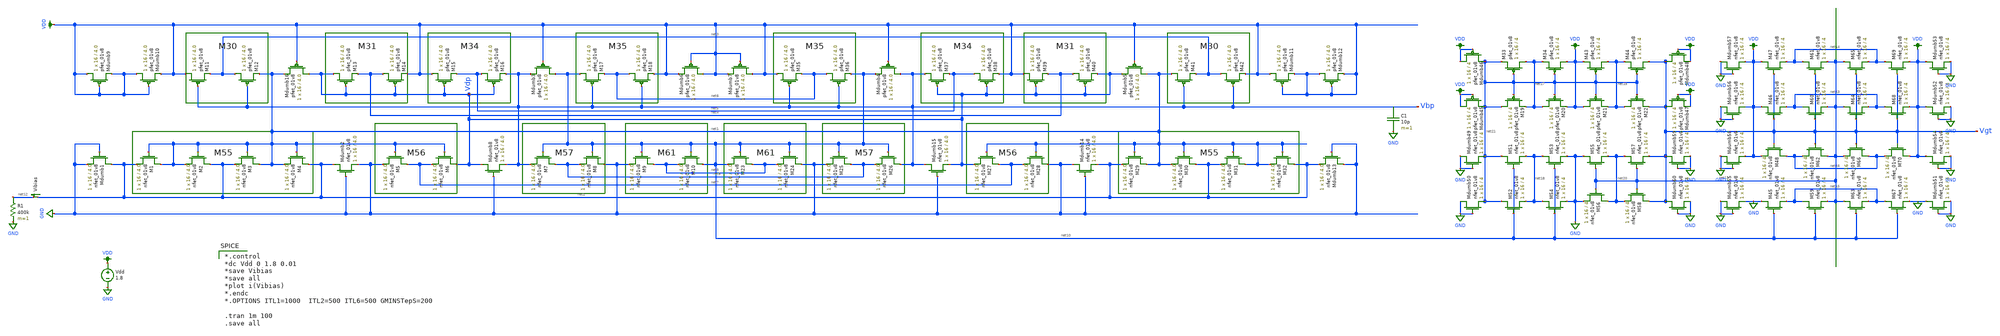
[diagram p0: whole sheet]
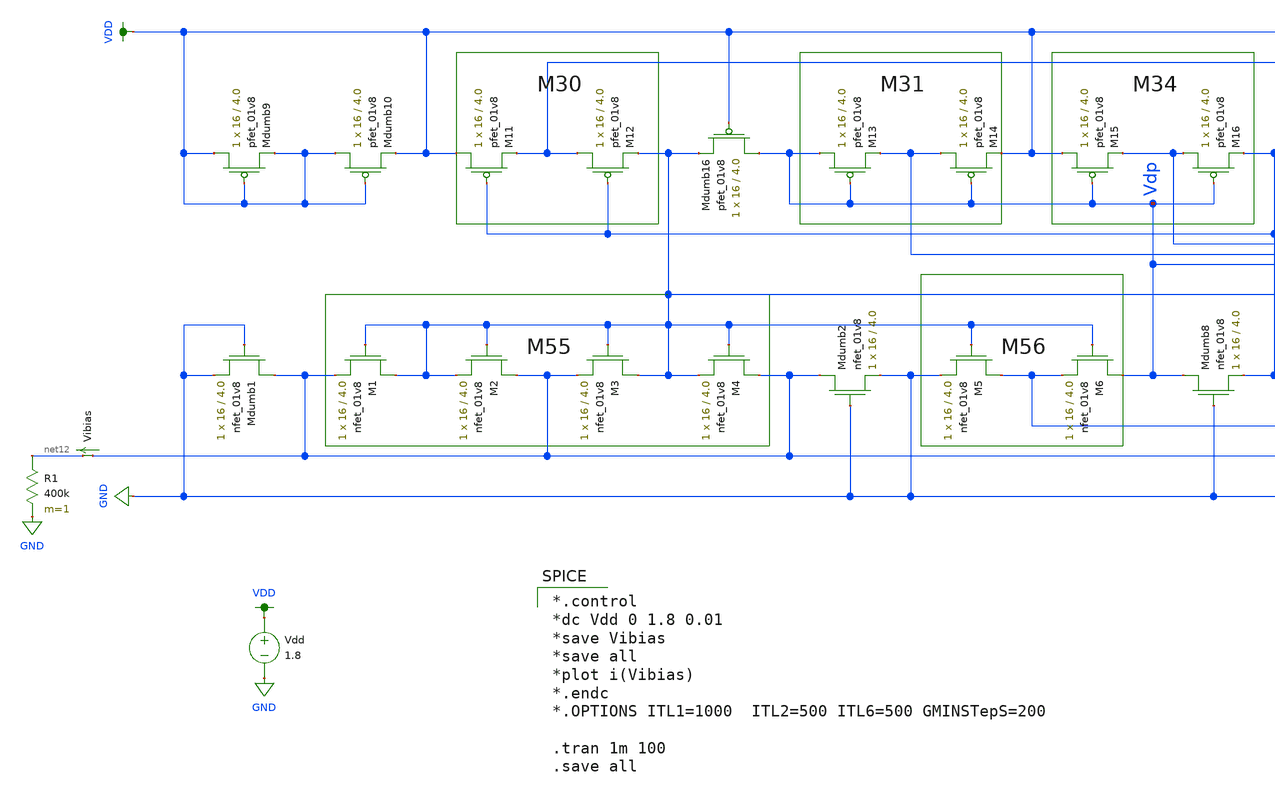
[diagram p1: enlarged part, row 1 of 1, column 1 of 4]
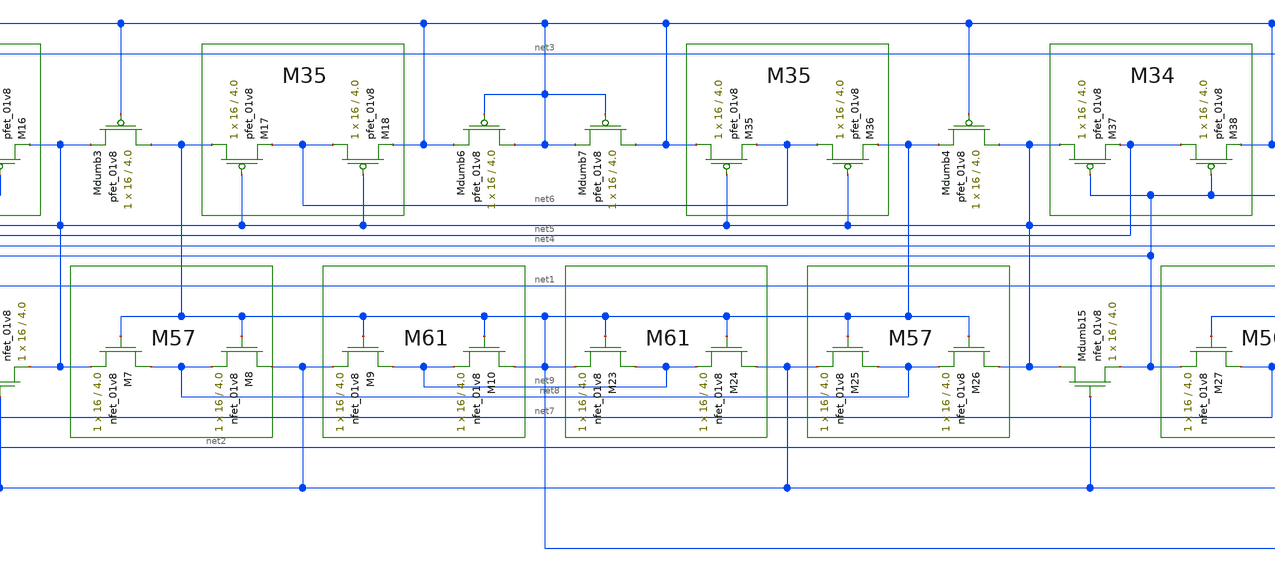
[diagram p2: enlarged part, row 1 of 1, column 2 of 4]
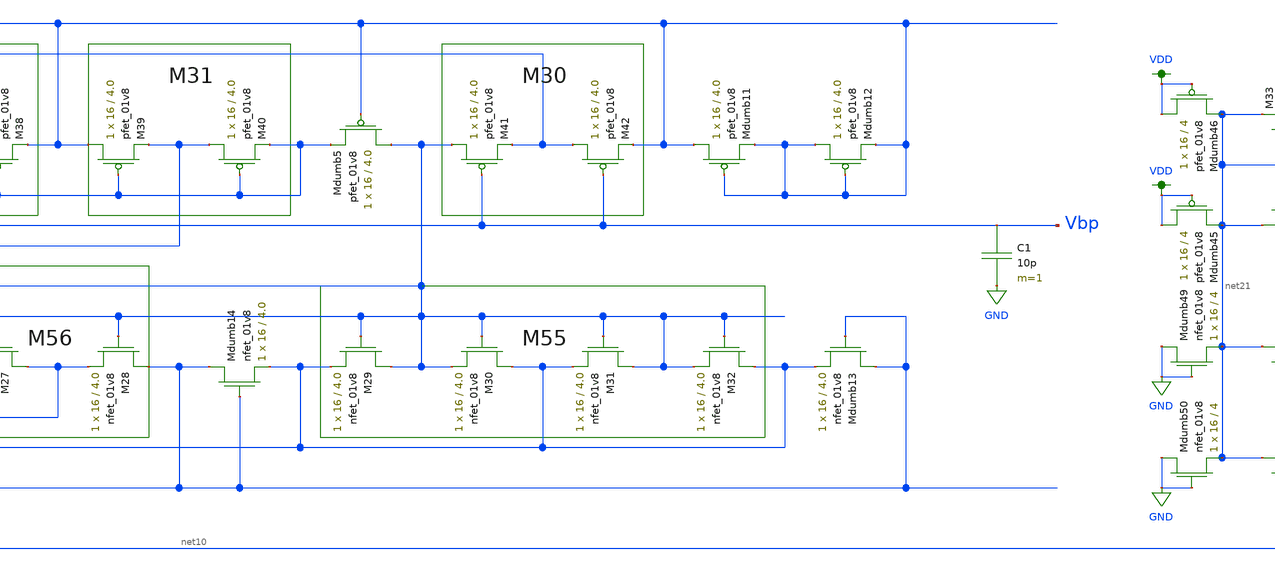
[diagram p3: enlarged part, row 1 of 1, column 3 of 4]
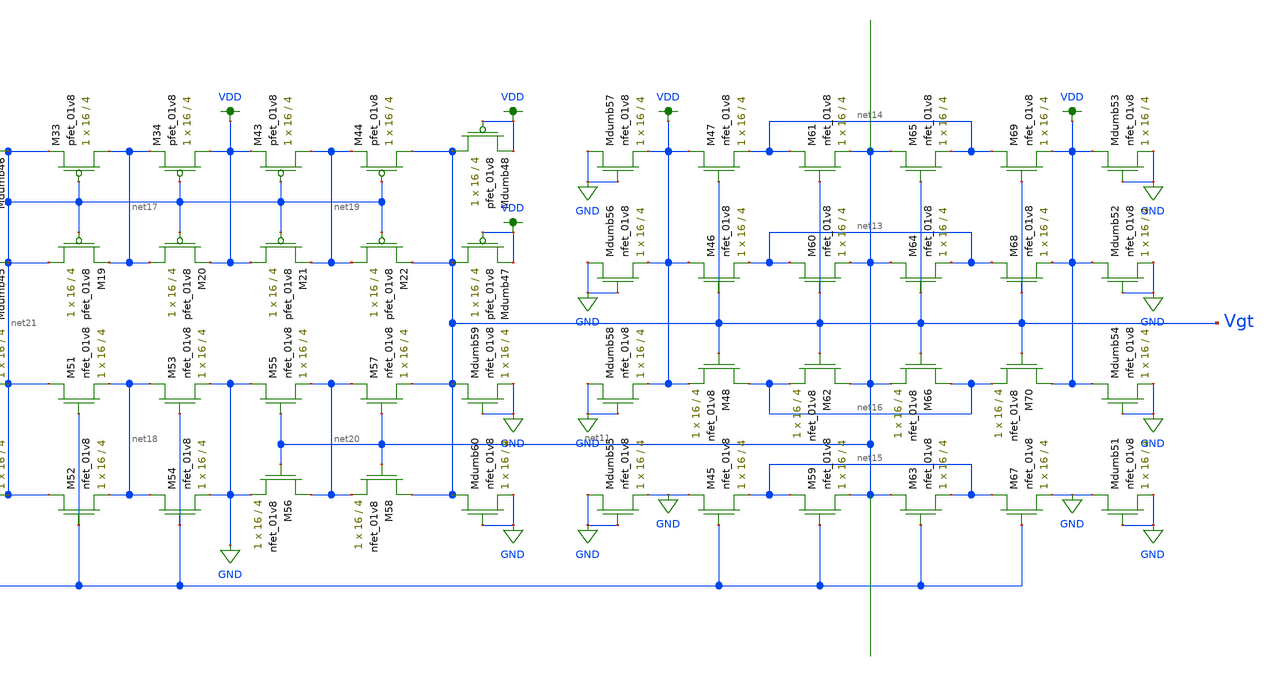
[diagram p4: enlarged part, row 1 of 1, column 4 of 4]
** sch_path: schematic/LDS/test/ibias_vgt.sch
**.subckt ibias_vgt
XM1 net1 net1 net2 GND sky130_fd_pr__nfet_01v8 L=4.0 W=16 nf=1 ad='int((nf+1)/2) * W/nf * 0.29' as='int((nf+2)/2) * W/nf * 0.29'
+ pd='2*int((nf+1)/2) * (W/nf + 0.29)' ps='2*int((nf+2)/2) * (W/nf + 0.29)' nrd='0.29 / W' nrs='0.29 / W'
+ sa=0 sb=0 sd=0 mult=1 m=1
XM2 net2 net1 net1 GND sky130_fd_pr__nfet_01v8 L=4.0 W=16 nf=1 ad='int((nf+1)/2) * W/nf * 0.29' as='int((nf+2)/2) * W/nf * 0.29'
+ pd='2*int((nf+1)/2) * (W/nf + 0.29)' ps='2*int((nf+2)/2) * (W/nf + 0.29)' nrd='0.29 / W' nrs='0.29 / W'
+ sa=0 sb=0 sd=0 mult=1 m=1
XM3 net1 net1 net2 GND sky130_fd_pr__nfet_01v8 L=4.0 W=16 nf=1 ad='int((nf+1)/2) * W/nf * 0.29' as='int((nf+2)/2) * W/nf * 0.29'
+ pd='2*int((nf+1)/2) * (W/nf + 0.29)' ps='2*int((nf+2)/2) * (W/nf + 0.29)' nrd='0.29 / W' nrs='0.29 / W'
+ sa=0 sb=0 sd=0 mult=1 m=1
XM4 net2 net1 net1 GND sky130_fd_pr__nfet_01v8 L=4.0 W=16 nf=1 ad='int((nf+1)/2) * W/nf * 0.29' as='int((nf+2)/2) * W/nf * 0.29'
+ pd='2*int((nf+1)/2) * (W/nf + 0.29)' ps='2*int((nf+2)/2) * (W/nf + 0.29)' nrd='0.29 / W' nrs='0.29 / W'
+ sa=0 sb=0 sd=0 mult=1 m=1
XM5 net7 net1 GND GND sky130_fd_pr__nfet_01v8 L=4.0 W=16 nf=1 ad='int((nf+1)/2) * W/nf * 0.29' as='int((nf+2)/2) * W/nf * 0.29'
+ pd='2*int((nf+1)/2) * (W/nf + 0.29)' ps='2*int((nf+2)/2) * (W/nf + 0.29)' nrd='0.29 / W' nrs='0.29 / W'
+ sa=0 sb=0 sd=0 mult=1 m=1
XM6 Vdp net1 net7 GND sky130_fd_pr__nfet_01v8 L=4.0 W=16 nf=1 ad='int((nf+1)/2) * W/nf * 0.29' as='int((nf+2)/2) * W/nf * 0.29'
+ pd='2*int((nf+1)/2) * (W/nf + 0.29)' ps='2*int((nf+2)/2) * (W/nf + 0.29)' nrd='0.29 / W' nrs='0.29 / W'
+ sa=0 sb=0 sd=0 mult=1 m=1
XM7 net8 net10 Vbp GND sky130_fd_pr__nfet_01v8 L=4.0 W=16 nf=1 ad='int((nf+1)/2) * W/nf * 0.29' as='int((nf+2)/2) * W/nf * 0.29'
+ pd='2*int((nf+1)/2) * (W/nf + 0.29)' ps='2*int((nf+2)/2) * (W/nf + 0.29)' nrd='0.29 / W' nrs='0.29 / W'
+ sa=0 sb=0 sd=0 mult=1 m=1
XM8 GND net10 net8 GND sky130_fd_pr__nfet_01v8 L=4.0 W=16 nf=1 ad='int((nf+1)/2) * W/nf * 0.29' as='int((nf+2)/2) * W/nf * 0.29'
+ pd='2*int((nf+1)/2) * (W/nf + 0.29)' ps='2*int((nf+2)/2) * (W/nf + 0.29)' nrd='0.29 / W' nrs='0.29 / W'
+ sa=0 sb=0 sd=0 mult=1 m=1
XM9 net9 net10 GND GND sky130_fd_pr__nfet_01v8 L=4.0 W=16 nf=1 ad='int((nf+1)/2) * W/nf * 0.29' as='int((nf+2)/2) * W/nf * 0.29'
+ pd='2*int((nf+1)/2) * (W/nf + 0.29)' ps='2*int((nf+2)/2) * (W/nf + 0.29)' nrd='0.29 / W' nrs='0.29 / W'
+ sa=0 sb=0 sd=0 mult=1 m=1
XM10 net10 net10 net9 GND sky130_fd_pr__nfet_01v8 L=4.0 W=16 nf=1 ad='int((nf+1)/2) * W/nf * 0.29' as='int((nf+2)/2) * W/nf * 0.29'
+ pd='2*int((nf+1)/2) * (W/nf + 0.29)' ps='2*int((nf+2)/2) * (W/nf + 0.29)' nrd='0.29 / W' nrs='0.29 / W'
+ sa=0 sb=0 sd=0 mult=1 m=1
XM11 VDD Vbp net3 VDD sky130_fd_pr__pfet_01v8 L=4.0 W=16 nf=1 ad='int((nf+1)/2) * W/nf * 0.29' as='int((nf+2)/2) * W/nf * 0.29'
+ pd='2*int((nf+1)/2) * (W/nf + 0.29)' ps='2*int((nf+2)/2) * (W/nf + 0.29)' nrd='0.29 / W' nrs='0.29 / W'
+ sa=0 sb=0 sd=0 mult=1 m=1
XM12 net3 Vbp net1 VDD sky130_fd_pr__pfet_01v8 L=4.0 W=16 nf=1 ad='int((nf+1)/2) * W/nf * 0.29' as='int((nf+2)/2) * W/nf * 0.29'
+ pd='2*int((nf+1)/2) * (W/nf + 0.29)' ps='2*int((nf+2)/2) * (W/nf + 0.29)' nrd='0.29 / W' nrs='0.29 / W'
+ sa=0 sb=0 sd=0 mult=1 m=1
XM13 Vdp Vdp net4 VDD sky130_fd_pr__pfet_01v8 L=4.0 W=16 nf=1 ad='int((nf+1)/2) * W/nf * 0.29' as='int((nf+2)/2) * W/nf * 0.29'
+ pd='2*int((nf+1)/2) * (W/nf + 0.29)' ps='2*int((nf+2)/2) * (W/nf + 0.29)' nrd='0.29 / W' nrs='0.29 / W'
+ sa=0 sb=0 sd=0 mult=1 m=1
XM14 net4 Vdp VDD VDD sky130_fd_pr__pfet_01v8 L=4.0 W=16 nf=1 ad='int((nf+1)/2) * W/nf * 0.29' as='int((nf+2)/2) * W/nf * 0.29'
+ pd='2*int((nf+1)/2) * (W/nf + 0.29)' ps='2*int((nf+2)/2) * (W/nf + 0.29)' nrd='0.29 / W' nrs='0.29 / W'
+ sa=0 sb=0 sd=0 mult=1 m=1
XM15 VDD Vdp net5 VDD sky130_fd_pr__pfet_01v8 L=4.0 W=16 nf=1 ad='int((nf+1)/2) * W/nf * 0.29' as='int((nf+2)/2) * W/nf * 0.29'
+ pd='2*int((nf+1)/2) * (W/nf + 0.29)' ps='2*int((nf+2)/2) * (W/nf + 0.29)' nrd='0.29 / W' nrs='0.29 / W'
+ sa=0 sb=0 sd=0 mult=1 m=1
XM16 net5 Vdp Vbp VDD sky130_fd_pr__pfet_01v8 L=4.0 W=16 nf=1 ad='int((nf+1)/2) * W/nf * 0.29' as='int((nf+2)/2) * W/nf * 0.29'
+ pd='2*int((nf+1)/2) * (W/nf + 0.29)' ps='2*int((nf+2)/2) * (W/nf + 0.29)' nrd='0.29 / W' nrs='0.29 / W'
+ sa=0 sb=0 sd=0 mult=1 m=1
XM17 net10 Vbp net6 VDD sky130_fd_pr__pfet_01v8 L=4.0 W=16 nf=1 ad='int((nf+1)/2) * W/nf * 0.29' as='int((nf+2)/2) * W/nf * 0.29'
+ pd='2*int((nf+1)/2) * (W/nf + 0.29)' ps='2*int((nf+2)/2) * (W/nf + 0.29)' nrd='0.29 / W' nrs='0.29 / W'
+ sa=0 sb=0 sd=0 mult=1 m=1
XM18 net6 Vbp VDD VDD sky130_fd_pr__pfet_01v8 L=4.0 W=16 nf=1 ad='int((nf+1)/2) * W/nf * 0.29' as='int((nf+2)/2) * W/nf * 0.29'
+ pd='2*int((nf+1)/2) * (W/nf + 0.29)' ps='2*int((nf+2)/2) * (W/nf + 0.29)' nrd='0.29 / W' nrs='0.29 / W'
+ sa=0 sb=0 sd=0 mult=1 m=1
XMdumb16 Vdp VDD net1 VDD sky130_fd_pr__pfet_01v8 L=4.0 W=16 nf=1 ad='int((nf+1)/2) * W/nf * 0.29' as='int((nf+2)/2) * W/nf * 0.29'
+ pd='2*int((nf+1)/2) * (W/nf + 0.29)' ps='2*int((nf+2)/2) * (W/nf + 0.29)' nrd='0.29 / W' nrs='0.29 / W'
+ sa=0 sb=0 sd=0 mult=1 m=1
XMdumb3 net10 VDD Vbp VDD sky130_fd_pr__pfet_01v8 L=4.0 W=16 nf=1 ad='int((nf+1)/2) * W/nf * 0.29' as='int((nf+2)/2) * W/nf * 0.29'
+ pd='2*int((nf+1)/2) * (W/nf + 0.29)' ps='2*int((nf+2)/2) * (W/nf + 0.29)' nrd='0.29 / W' nrs='0.29 / W'
+ sa=0 sb=0 sd=0 mult=1 m=1
XMdumb2 net2 GND GND GND sky130_fd_pr__nfet_01v8 L=4.0 W=16 nf=1 ad='int((nf+1)/2) * W/nf * 0.29' as='int((nf+2)/2) * W/nf * 0.29'
+ pd='2*int((nf+1)/2) * (W/nf + 0.29)' ps='2*int((nf+2)/2) * (W/nf + 0.29)' nrd='0.29 / W' nrs='0.29 / W'
+ sa=0 sb=0 sd=0 mult=1 m=1
XMdumb8 Vdp GND Vbp GND sky130_fd_pr__nfet_01v8 L=4.0 W=16 nf=1 ad='int((nf+1)/2) * W/nf * 0.29' as='int((nf+2)/2) * W/nf * 0.29'
+ pd='2*int((nf+1)/2) * (W/nf + 0.29)' ps='2*int((nf+2)/2) * (W/nf + 0.29)' nrd='0.29 / W' nrs='0.29 / W'
+ sa=0 sb=0 sd=0 mult=1 m=1
XM23 net9 net10 net10 GND sky130_fd_pr__nfet_01v8 L=4.0 W=16 nf=1 ad='int((nf+1)/2) * W/nf * 0.29' as='int((nf+2)/2) * W/nf * 0.29'
+ pd='2*int((nf+1)/2) * (W/nf + 0.29)' ps='2*int((nf+2)/2) * (W/nf + 0.29)' nrd='0.29 / W' nrs='0.29 / W'
+ sa=0 sb=0 sd=0 mult=1 m=1
XM24 GND net10 net9 GND sky130_fd_pr__nfet_01v8 L=4.0 W=16 nf=1 ad='int((nf+1)/2) * W/nf * 0.29' as='int((nf+2)/2) * W/nf * 0.29'
+ pd='2*int((nf+1)/2) * (W/nf + 0.29)' ps='2*int((nf+2)/2) * (W/nf + 0.29)' nrd='0.29 / W' nrs='0.29 / W'
+ sa=0 sb=0 sd=0 mult=1 m=1
XM25 net8 net10 GND GND sky130_fd_pr__nfet_01v8 L=4.0 W=16 nf=1 ad='int((nf+1)/2) * W/nf * 0.29' as='int((nf+2)/2) * W/nf * 0.29'
+ pd='2*int((nf+1)/2) * (W/nf + 0.29)' ps='2*int((nf+2)/2) * (W/nf + 0.29)' nrd='0.29 / W' nrs='0.29 / W'
+ sa=0 sb=0 sd=0 mult=1 m=1
XM26 Vbp net10 net8 GND sky130_fd_pr__nfet_01v8 L=4.0 W=16 nf=1 ad='int((nf+1)/2) * W/nf * 0.29' as='int((nf+2)/2) * W/nf * 0.29'
+ pd='2*int((nf+1)/2) * (W/nf + 0.29)' ps='2*int((nf+2)/2) * (W/nf + 0.29)' nrd='0.29 / W' nrs='0.29 / W'
+ sa=0 sb=0 sd=0 mult=1 m=1
XM27 net7 net1 Vdp GND sky130_fd_pr__nfet_01v8 L=4.0 W=16 nf=1 ad='int((nf+1)/2) * W/nf * 0.29' as='int((nf+2)/2) * W/nf * 0.29'
+ pd='2*int((nf+1)/2) * (W/nf + 0.29)' ps='2*int((nf+2)/2) * (W/nf + 0.29)' nrd='0.29 / W' nrs='0.29 / W'
+ sa=0 sb=0 sd=0 mult=1 m=1
XM28 GND net1 net7 GND sky130_fd_pr__nfet_01v8 L=4.0 W=16 nf=1 ad='int((nf+1)/2) * W/nf * 0.29' as='int((nf+2)/2) * W/nf * 0.29'
+ pd='2*int((nf+1)/2) * (W/nf + 0.29)' ps='2*int((nf+2)/2) * (W/nf + 0.29)' nrd='0.29 / W' nrs='0.29 / W'
+ sa=0 sb=0 sd=0 mult=1 m=1
XM29 net1 net1 net2 GND sky130_fd_pr__nfet_01v8 L=4.0 W=16 nf=1 ad='int((nf+1)/2) * W/nf * 0.29' as='int((nf+2)/2) * W/nf * 0.29'
+ pd='2*int((nf+1)/2) * (W/nf + 0.29)' ps='2*int((nf+2)/2) * (W/nf + 0.29)' nrd='0.29 / W' nrs='0.29 / W'
+ sa=0 sb=0 sd=0 mult=1 m=1
XM30 net2 net1 net1 GND sky130_fd_pr__nfet_01v8 L=4.0 W=16 nf=1 ad='int((nf+1)/2) * W/nf * 0.29' as='int((nf+2)/2) * W/nf * 0.29'
+ pd='2*int((nf+1)/2) * (W/nf + 0.29)' ps='2*int((nf+2)/2) * (W/nf + 0.29)' nrd='0.29 / W' nrs='0.29 / W'
+ sa=0 sb=0 sd=0 mult=1 m=1
XM31 net1 net1 net2 GND sky130_fd_pr__nfet_01v8 L=4.0 W=16 nf=1 ad='int((nf+1)/2) * W/nf * 0.29' as='int((nf+2)/2) * W/nf * 0.29'
+ pd='2*int((nf+1)/2) * (W/nf + 0.29)' ps='2*int((nf+2)/2) * (W/nf + 0.29)' nrd='0.29 / W' nrs='0.29 / W'
+ sa=0 sb=0 sd=0 mult=1 m=1
XM32 net2 net1 net1 GND sky130_fd_pr__nfet_01v8 L=4.0 W=16 nf=1 ad='int((nf+1)/2) * W/nf * 0.29' as='int((nf+2)/2) * W/nf * 0.29'
+ pd='2*int((nf+1)/2) * (W/nf + 0.29)' ps='2*int((nf+2)/2) * (W/nf + 0.29)' nrd='0.29 / W' nrs='0.29 / W'
+ sa=0 sb=0 sd=0 mult=1 m=1
XMdumb15 Vbp GND Vdp GND sky130_fd_pr__nfet_01v8 L=4.0 W=16 nf=1 ad='int((nf+1)/2) * W/nf * 0.29' as='int((nf+2)/2) * W/nf * 0.29'
+ pd='2*int((nf+1)/2) * (W/nf + 0.29)' ps='2*int((nf+2)/2) * (W/nf + 0.29)' nrd='0.29 / W' nrs='0.29 / W'
+ sa=0 sb=0 sd=0 mult=1 m=1
XMdumb14 GND GND net2 GND sky130_fd_pr__nfet_01v8 L=4.0 W=16 nf=1 ad='int((nf+1)/2) * W/nf * 0.29' as='int((nf+2)/2) * W/nf * 0.29'
+ pd='2*int((nf+1)/2) * (W/nf + 0.29)' ps='2*int((nf+2)/2) * (W/nf + 0.29)' nrd='0.29 / W' nrs='0.29 / W'
+ sa=0 sb=0 sd=0 mult=1 m=1
XM35 VDD Vbp net6 VDD sky130_fd_pr__pfet_01v8 L=4.0 W=16 nf=1 ad='int((nf+1)/2) * W/nf * 0.29' as='int((nf+2)/2) * W/nf * 0.29'
+ pd='2*int((nf+1)/2) * (W/nf + 0.29)' ps='2*int((nf+2)/2) * (W/nf + 0.29)' nrd='0.29 / W' nrs='0.29 / W'
+ sa=0 sb=0 sd=0 mult=1 m=1
XM36 net6 Vbp net10 VDD sky130_fd_pr__pfet_01v8 L=4.0 W=16 nf=1 ad='int((nf+1)/2) * W/nf * 0.29' as='int((nf+2)/2) * W/nf * 0.29'
+ pd='2*int((nf+1)/2) * (W/nf + 0.29)' ps='2*int((nf+2)/2) * (W/nf + 0.29)' nrd='0.29 / W' nrs='0.29 / W'
+ sa=0 sb=0 sd=0 mult=1 m=1
XM37 Vbp Vdp net5 VDD sky130_fd_pr__pfet_01v8 L=4.0 W=16 nf=1 ad='int((nf+1)/2) * W/nf * 0.29' as='int((nf+2)/2) * W/nf * 0.29'
+ pd='2*int((nf+1)/2) * (W/nf + 0.29)' ps='2*int((nf+2)/2) * (W/nf + 0.29)' nrd='0.29 / W' nrs='0.29 / W'
+ sa=0 sb=0 sd=0 mult=1 m=1
XM38 net5 Vdp VDD VDD sky130_fd_pr__pfet_01v8 L=4.0 W=16 nf=1 ad='int((nf+1)/2) * W/nf * 0.29' as='int((nf+2)/2) * W/nf * 0.29'
+ pd='2*int((nf+1)/2) * (W/nf + 0.29)' ps='2*int((nf+2)/2) * (W/nf + 0.29)' nrd='0.29 / W' nrs='0.29 / W'
+ sa=0 sb=0 sd=0 mult=1 m=1
XM39 VDD Vdp net4 VDD sky130_fd_pr__pfet_01v8 L=4.0 W=16 nf=1 ad='int((nf+1)/2) * W/nf * 0.29' as='int((nf+2)/2) * W/nf * 0.29'
+ pd='2*int((nf+1)/2) * (W/nf + 0.29)' ps='2*int((nf+2)/2) * (W/nf + 0.29)' nrd='0.29 / W' nrs='0.29 / W'
+ sa=0 sb=0 sd=0 mult=1 m=1
XM40 net4 Vdp Vdp VDD sky130_fd_pr__pfet_01v8 L=4.0 W=16 nf=1 ad='int((nf+1)/2) * W/nf * 0.29' as='int((nf+2)/2) * W/nf * 0.29'
+ pd='2*int((nf+1)/2) * (W/nf + 0.29)' ps='2*int((nf+2)/2) * (W/nf + 0.29)' nrd='0.29 / W' nrs='0.29 / W'
+ sa=0 sb=0 sd=0 mult=1 m=1
XM41 net1 Vbp net3 VDD sky130_fd_pr__pfet_01v8 L=4.0 W=16 nf=1 ad='int((nf+1)/2) * W/nf * 0.29' as='int((nf+2)/2) * W/nf * 0.29'
+ pd='2*int((nf+1)/2) * (W/nf + 0.29)' ps='2*int((nf+2)/2) * (W/nf + 0.29)' nrd='0.29 / W' nrs='0.29 / W'
+ sa=0 sb=0 sd=0 mult=1 m=1
XM42 net3 Vbp VDD VDD sky130_fd_pr__pfet_01v8 L=4.0 W=16 nf=1 ad='int((nf+1)/2) * W/nf * 0.29' as='int((nf+2)/2) * W/nf * 0.29'
+ pd='2*int((nf+1)/2) * (W/nf + 0.29)' ps='2*int((nf+2)/2) * (W/nf + 0.29)' nrd='0.29 / W' nrs='0.29 / W'
+ sa=0 sb=0 sd=0 mult=1 m=1
XMdumb4 Vbp VDD net10 VDD sky130_fd_pr__pfet_01v8 L=4.0 W=16 nf=1 ad='int((nf+1)/2) * W/nf * 0.29' as='int((nf+2)/2) * W/nf * 0.29'
+ pd='2*int((nf+1)/2) * (W/nf + 0.29)' ps='2*int((nf+2)/2) * (W/nf + 0.29)' nrd='0.29 / W' nrs='0.29 / W'
+ sa=0 sb=0 sd=0 mult=1 m=1
XMdumb5 net1 VDD Vdp VDD sky130_fd_pr__pfet_01v8 L=4.0 W=16 nf=1 ad='int((nf+1)/2) * W/nf * 0.29' as='int((nf+2)/2) * W/nf * 0.29'
+ pd='2*int((nf+1)/2) * (W/nf + 0.29)' ps='2*int((nf+2)/2) * (W/nf + 0.29)' nrd='0.29 / W' nrs='0.29 / W'
+ sa=0 sb=0 sd=0 mult=1 m=1
XMdumb6 VDD VDD VDD VDD sky130_fd_pr__pfet_01v8 L=4.0 W=16 nf=1 ad='int((nf+1)/2) * W/nf * 0.29' as='int((nf+2)/2) * W/nf * 0.29'
+ pd='2*int((nf+1)/2) * (W/nf + 0.29)' ps='2*int((nf+2)/2) * (W/nf + 0.29)' nrd='0.29 / W' nrs='0.29 / W'
+ sa=0 sb=0 sd=0 mult=1 m=1
XMdumb7 VDD VDD VDD VDD sky130_fd_pr__pfet_01v8 L=4.0 W=16 nf=1 ad='int((nf+1)/2) * W/nf * 0.29' as='int((nf+2)/2) * W/nf * 0.29'
+ pd='2*int((nf+1)/2) * (W/nf + 0.29)' ps='2*int((nf+2)/2) * (W/nf + 0.29)' nrd='0.29 / W' nrs='0.29 / W'
+ sa=0 sb=0 sd=0 mult=1 m=1
XMdumb11 VDD VDD VDD VDD sky130_fd_pr__pfet_01v8 L=4.0 W=16 nf=1 ad='int((nf+1)/2) * W/nf * 0.29' as='int((nf+2)/2) * W/nf * 0.29'
+ pd='2*int((nf+1)/2) * (W/nf + 0.29)' ps='2*int((nf+2)/2) * (W/nf + 0.29)' nrd='0.29 / W' nrs='0.29 / W'
+ sa=0 sb=0 sd=0 mult=1 m=1
XMdumb12 VDD VDD VDD VDD sky130_fd_pr__pfet_01v8 L=4.0 W=16 nf=1 ad='int((nf+1)/2) * W/nf * 0.29' as='int((nf+2)/2) * W/nf * 0.29'
+ pd='2*int((nf+1)/2) * (W/nf + 0.29)' ps='2*int((nf+2)/2) * (W/nf + 0.29)' nrd='0.29 / W' nrs='0.29 / W'
+ sa=0 sb=0 sd=0 mult=1 m=1
XMdumb13 GND GND net2 GND sky130_fd_pr__nfet_01v8 L=4.0 W=16 nf=1 ad='int((nf+1)/2) * W/nf * 0.29' as='int((nf+2)/2) * W/nf * 0.29'
+ pd='2*int((nf+1)/2) * (W/nf + 0.29)' ps='2*int((nf+2)/2) * (W/nf + 0.29)' nrd='0.29 / W' nrs='0.29 / W'
+ sa=0 sb=0 sd=0 mult=1 m=1
XMdumb1 net2 GND GND GND sky130_fd_pr__nfet_01v8 L=4.0 W=16 nf=1 ad='int((nf+1)/2) * W/nf * 0.29' as='int((nf+2)/2) * W/nf * 0.29'
+ pd='2*int((nf+1)/2) * (W/nf + 0.29)' ps='2*int((nf+2)/2) * (W/nf + 0.29)' nrd='0.29 / W' nrs='0.29 / W'
+ sa=0 sb=0 sd=0 mult=1 m=1
XMdumb10 VDD VDD VDD VDD sky130_fd_pr__pfet_01v8 L=4.0 W=16 nf=1 ad='int((nf+1)/2) * W/nf * 0.29' as='int((nf+2)/2) * W/nf * 0.29'
+ pd='2*int((nf+1)/2) * (W/nf + 0.29)' ps='2*int((nf+2)/2) * (W/nf + 0.29)' nrd='0.29 / W' nrs='0.29 / W'
+ sa=0 sb=0 sd=0 mult=1 m=1
XMdumb9 VDD VDD VDD VDD sky130_fd_pr__pfet_01v8 L=4.0 W=16 nf=1 ad='int((nf+1)/2) * W/nf * 0.29' as='int((nf+2)/2) * W/nf * 0.29'
+ pd='2*int((nf+1)/2) * (W/nf + 0.29)' ps='2*int((nf+2)/2) * (W/nf + 0.29)' nrd='0.29 / W' nrs='0.29 / W'
+ sa=0 sb=0 sd=0 mult=1 m=1
Vdd VDD GND 1.8
R1 net12 GND 400k m=1
Vibias net2 net12 0
.save i(vibias)
XM45 GND net10 net15 GND sky130_fd_pr__nfet_01v8 L=4 W=16 nf=1 ad='int((nf+1)/2) * W/nf * 0.29' as='int((nf+2)/2) * W/nf * 0.29'
+ pd='2*int((nf+1)/2) * (W/nf + 0.29)' ps='2*int((nf+2)/2) * (W/nf + 0.29)' nrd='0.29 / W' nrs='0.29 / W'
+ sa=0 sb=0 sd=0 mult=1 m=1
XM46 VDD Vgt net13 GND sky130_fd_pr__nfet_01v8 L=4 W=16 nf=1 ad='int((nf+1)/2) * W/nf * 0.29' as='int((nf+2)/2) * W/nf * 0.29'
+ pd='2*int((nf+1)/2) * (W/nf + 0.29)' ps='2*int((nf+2)/2) * (W/nf + 0.29)' nrd='0.29 / W' nrs='0.29 / W'
+ sa=0 sb=0 sd=0 mult=1 m=1
XM47 VDD Vgt net14 GND sky130_fd_pr__nfet_01v8 L=4 W=16 nf=1 ad='int((nf+1)/2) * W/nf * 0.29' as='int((nf+2)/2) * W/nf * 0.29'
+ pd='2*int((nf+1)/2) * (W/nf + 0.29)' ps='2*int((nf+2)/2) * (W/nf + 0.29)' nrd='0.29 / W' nrs='0.29 / W'
+ sa=0 sb=0 sd=0 mult=1 m=1
XM48 net16 Vgt VDD GND sky130_fd_pr__nfet_01v8 L=4 W=16 nf=1 ad='int((nf+1)/2) * W/nf * 0.29' as='int((nf+2)/2) * W/nf * 0.29'
+ pd='2*int((nf+1)/2) * (W/nf + 0.29)' ps='2*int((nf+2)/2) * (W/nf + 0.29)' nrd='0.29 / W' nrs='0.29 / W'
+ sa=0 sb=0 sd=0 mult=1 m=1
XMdumb51 GND GND GND GND sky130_fd_pr__nfet_01v8 L=4 W=16 nf=1 ad='int((nf+1)/2) * W/nf * 0.29' as='int((nf+2)/2) * W/nf * 0.29'
+ pd='2*int((nf+1)/2) * (W/nf + 0.29)' ps='2*int((nf+2)/2) * (W/nf + 0.29)' nrd='0.29 / W' nrs='0.29 / W'
+ sa=0 sb=0 sd=0 mult=1 m=1
XMdumb52 VDD GND GND GND sky130_fd_pr__nfet_01v8 L=4 W=16 nf=1 ad='int((nf+1)/2) * W/nf * 0.29' as='int((nf+2)/2) * W/nf * 0.29'
+ pd='2*int((nf+1)/2) * (W/nf + 0.29)' ps='2*int((nf+2)/2) * (W/nf + 0.29)' nrd='0.29 / W' nrs='0.29 / W'
+ sa=0 sb=0 sd=0 mult=1 m=1
XMdumb53 VDD GND GND GND sky130_fd_pr__nfet_01v8 L=4 W=16 nf=1 ad='int((nf+1)/2) * W/nf * 0.29' as='int((nf+2)/2) * W/nf * 0.29'
+ pd='2*int((nf+1)/2) * (W/nf + 0.29)' ps='2*int((nf+2)/2) * (W/nf + 0.29)' nrd='0.29 / W' nrs='0.29 / W'
+ sa=0 sb=0 sd=0 mult=1 m=1
XMdumb54 VDD GND GND GND sky130_fd_pr__nfet_01v8 L=4 W=16 nf=1 ad='int((nf+1)/2) * W/nf * 0.29' as='int((nf+2)/2) * W/nf * 0.29'
+ pd='2*int((nf+1)/2) * (W/nf + 0.29)' ps='2*int((nf+2)/2) * (W/nf + 0.29)' nrd='0.29 / W' nrs='0.29 / W'
+ sa=0 sb=0 sd=0 mult=1 m=1
XMdumb55 GND GND GND GND sky130_fd_pr__nfet_01v8 L=4 W=16 nf=1 ad='int((nf+1)/2) * W/nf * 0.29' as='int((nf+2)/2) * W/nf * 0.29'
+ pd='2*int((nf+1)/2) * (W/nf + 0.29)' ps='2*int((nf+2)/2) * (W/nf + 0.29)' nrd='0.29 / W' nrs='0.29 / W'
+ sa=0 sb=0 sd=0 mult=1 m=1
XMdumb56 GND GND VDD GND sky130_fd_pr__nfet_01v8 L=4 W=16 nf=1 ad='int((nf+1)/2) * W/nf * 0.29' as='int((nf+2)/2) * W/nf * 0.29'
+ pd='2*int((nf+1)/2) * (W/nf + 0.29)' ps='2*int((nf+2)/2) * (W/nf + 0.29)' nrd='0.29 / W' nrs='0.29 / W'
+ sa=0 sb=0 sd=0 mult=1 m=1
XMdumb57 GND GND VDD GND sky130_fd_pr__nfet_01v8 L=4 W=16 nf=1 ad='int((nf+1)/2) * W/nf * 0.29' as='int((nf+2)/2) * W/nf * 0.29'
+ pd='2*int((nf+1)/2) * (W/nf + 0.29)' ps='2*int((nf+2)/2) * (W/nf + 0.29)' nrd='0.29 / W' nrs='0.29 / W'
+ sa=0 sb=0 sd=0 mult=1 m=1
XMdumb58 GND GND VDD GND sky130_fd_pr__nfet_01v8 L=4 W=16 nf=1 ad='int((nf+1)/2) * W/nf * 0.29' as='int((nf+2)/2) * W/nf * 0.29'
+ pd='2*int((nf+1)/2) * (W/nf + 0.29)' ps='2*int((nf+2)/2) * (W/nf + 0.29)' nrd='0.29 / W' nrs='0.29 / W'
+ sa=0 sb=0 sd=0 mult=1 m=1
XM59 net15 net10 net11 GND sky130_fd_pr__nfet_01v8 L=4 W=16 nf=1 ad='int((nf+1)/2) * W/nf * 0.29' as='int((nf+2)/2) * W/nf * 0.29'
+ pd='2*int((nf+1)/2) * (W/nf + 0.29)' ps='2*int((nf+2)/2) * (W/nf + 0.29)' nrd='0.29 / W' nrs='0.29 / W'
+ sa=0 sb=0 sd=0 mult=1 m=1
XM60 net13 Vgt net11 GND sky130_fd_pr__nfet_01v8 L=4 W=16 nf=1 ad='int((nf+1)/2) * W/nf * 0.29' as='int((nf+2)/2) * W/nf * 0.29'
+ pd='2*int((nf+1)/2) * (W/nf + 0.29)' ps='2*int((nf+2)/2) * (W/nf + 0.29)' nrd='0.29 / W' nrs='0.29 / W'
+ sa=0 sb=0 sd=0 mult=1 m=1
XM61 net14 Vgt net11 GND sky130_fd_pr__nfet_01v8 L=4 W=16 nf=1 ad='int((nf+1)/2) * W/nf * 0.29' as='int((nf+2)/2) * W/nf * 0.29'
+ pd='2*int((nf+1)/2) * (W/nf + 0.29)' ps='2*int((nf+2)/2) * (W/nf + 0.29)' nrd='0.29 / W' nrs='0.29 / W'
+ sa=0 sb=0 sd=0 mult=1 m=1
XM62 net11 Vgt net16 GND sky130_fd_pr__nfet_01v8 L=4 W=16 nf=1 ad='int((nf+1)/2) * W/nf * 0.29' as='int((nf+2)/2) * W/nf * 0.29'
+ pd='2*int((nf+1)/2) * (W/nf + 0.29)' ps='2*int((nf+2)/2) * (W/nf + 0.29)' nrd='0.29 / W' nrs='0.29 / W'
+ sa=0 sb=0 sd=0 mult=1 m=1
XM63 net11 net10 net15 GND sky130_fd_pr__nfet_01v8 L=4 W=16 nf=1 ad='int((nf+1)/2) * W/nf * 0.29' as='int((nf+2)/2) * W/nf * 0.29'
+ pd='2*int((nf+1)/2) * (W/nf + 0.29)' ps='2*int((nf+2)/2) * (W/nf + 0.29)' nrd='0.29 / W' nrs='0.29 / W'
+ sa=0 sb=0 sd=0 mult=1 m=1
XM64 net11 Vgt net13 GND sky130_fd_pr__nfet_01v8 L=4 W=16 nf=1 ad='int((nf+1)/2) * W/nf * 0.29' as='int((nf+2)/2) * W/nf * 0.29'
+ pd='2*int((nf+1)/2) * (W/nf + 0.29)' ps='2*int((nf+2)/2) * (W/nf + 0.29)' nrd='0.29 / W' nrs='0.29 / W'
+ sa=0 sb=0 sd=0 mult=1 m=1
XM65 net11 Vgt net14 GND sky130_fd_pr__nfet_01v8 L=4 W=16 nf=1 ad='int((nf+1)/2) * W/nf * 0.29' as='int((nf+2)/2) * W/nf * 0.29'
+ pd='2*int((nf+1)/2) * (W/nf + 0.29)' ps='2*int((nf+2)/2) * (W/nf + 0.29)' nrd='0.29 / W' nrs='0.29 / W'
+ sa=0 sb=0 sd=0 mult=1 m=1
XM66 net16 Vgt net11 GND sky130_fd_pr__nfet_01v8 L=4 W=16 nf=1 ad='int((nf+1)/2) * W/nf * 0.29' as='int((nf+2)/2) * W/nf * 0.29'
+ pd='2*int((nf+1)/2) * (W/nf + 0.29)' ps='2*int((nf+2)/2) * (W/nf + 0.29)' nrd='0.29 / W' nrs='0.29 / W'
+ sa=0 sb=0 sd=0 mult=1 m=1
XM67 net15 net10 GND GND sky130_fd_pr__nfet_01v8 L=4 W=16 nf=1 ad='int((nf+1)/2) * W/nf * 0.29' as='int((nf+2)/2) * W/nf * 0.29'
+ pd='2*int((nf+1)/2) * (W/nf + 0.29)' ps='2*int((nf+2)/2) * (W/nf + 0.29)' nrd='0.29 / W' nrs='0.29 / W'
+ sa=0 sb=0 sd=0 mult=1 m=1
XM68 net13 Vgt VDD GND sky130_fd_pr__nfet_01v8 L=4 W=16 nf=1 ad='int((nf+1)/2) * W/nf * 0.29' as='int((nf+2)/2) * W/nf * 0.29'
+ pd='2*int((nf+1)/2) * (W/nf + 0.29)' ps='2*int((nf+2)/2) * (W/nf + 0.29)' nrd='0.29 / W' nrs='0.29 / W'
+ sa=0 sb=0 sd=0 mult=1 m=1
XM69 net14 Vgt VDD GND sky130_fd_pr__nfet_01v8 L=4 W=16 nf=1 ad='int((nf+1)/2) * W/nf * 0.29' as='int((nf+2)/2) * W/nf * 0.29'
+ pd='2*int((nf+1)/2) * (W/nf + 0.29)' ps='2*int((nf+2)/2) * (W/nf + 0.29)' nrd='0.29 / W' nrs='0.29 / W'
+ sa=0 sb=0 sd=0 mult=1 m=1
XM70 VDD Vgt net16 GND sky130_fd_pr__nfet_01v8 L=4 W=16 nf=1 ad='int((nf+1)/2) * W/nf * 0.29' as='int((nf+2)/2) * W/nf * 0.29'
+ pd='2*int((nf+1)/2) * (W/nf + 0.29)' ps='2*int((nf+2)/2) * (W/nf + 0.29)' nrd='0.29 / W' nrs='0.29 / W'
+ sa=0 sb=0 sd=0 mult=1 m=1
XM19 net21 net21 net17 VDD sky130_fd_pr__pfet_01v8 L=4 W=16 nf=1 ad='int((nf+1)/2) * W/nf * 0.29' as='int((nf+2)/2) * W/nf * 0.29'
+ pd='2*int((nf+1)/2) * (W/nf + 0.29)' ps='2*int((nf+2)/2) * (W/nf + 0.29)' nrd='0.29 / W' nrs='0.29 / W'
+ sa=0 sb=0 sd=0 mult=1 m=1
XM20 net17 net21 VDD VDD sky130_fd_pr__pfet_01v8 L=4 W=16 nf=1 ad='int((nf+1)/2) * W/nf * 0.29' as='int((nf+2)/2) * W/nf * 0.29'
+ pd='2*int((nf+1)/2) * (W/nf + 0.29)' ps='2*int((nf+2)/2) * (W/nf + 0.29)' nrd='0.29 / W' nrs='0.29 / W'
+ sa=0 sb=0 sd=0 mult=1 m=1
XM21 VDD net21 net19 VDD sky130_fd_pr__pfet_01v8 L=4 W=16 nf=1 ad='int((nf+1)/2) * W/nf * 0.29' as='int((nf+2)/2) * W/nf * 0.29'
+ pd='2*int((nf+1)/2) * (W/nf + 0.29)' ps='2*int((nf+2)/2) * (W/nf + 0.29)' nrd='0.29 / W' nrs='0.29 / W'
+ sa=0 sb=0 sd=0 mult=1 m=1
XM22 net19 net21 Vgt VDD sky130_fd_pr__pfet_01v8 L=4 W=16 nf=1 ad='int((nf+1)/2) * W/nf * 0.29' as='int((nf+2)/2) * W/nf * 0.29'
+ pd='2*int((nf+1)/2) * (W/nf + 0.29)' ps='2*int((nf+2)/2) * (W/nf + 0.29)' nrd='0.29 / W' nrs='0.29 / W'
+ sa=0 sb=0 sd=0 mult=1 m=1
XM33 net17 net21 net21 VDD sky130_fd_pr__pfet_01v8 L=4 W=16 nf=1 ad='int((nf+1)/2) * W/nf * 0.29' as='int((nf+2)/2) * W/nf * 0.29'
+ pd='2*int((nf+1)/2) * (W/nf + 0.29)' ps='2*int((nf+2)/2) * (W/nf + 0.29)' nrd='0.29 / W' nrs='0.29 / W'
+ sa=0 sb=0 sd=0 mult=1 m=1
XM34 VDD net21 net17 VDD sky130_fd_pr__pfet_01v8 L=4 W=16 nf=1 ad='int((nf+1)/2) * W/nf * 0.29' as='int((nf+2)/2) * W/nf * 0.29'
+ pd='2*int((nf+1)/2) * (W/nf + 0.29)' ps='2*int((nf+2)/2) * (W/nf + 0.29)' nrd='0.29 / W' nrs='0.29 / W'
+ sa=0 sb=0 sd=0 mult=1 m=1
XM43 net19 net21 VDD VDD sky130_fd_pr__pfet_01v8 L=4 W=16 nf=1 ad='int((nf+1)/2) * W/nf * 0.29' as='int((nf+2)/2) * W/nf * 0.29'
+ pd='2*int((nf+1)/2) * (W/nf + 0.29)' ps='2*int((nf+2)/2) * (W/nf + 0.29)' nrd='0.29 / W' nrs='0.29 / W'
+ sa=0 sb=0 sd=0 mult=1 m=1
XM44 Vgt net21 net19 VDD sky130_fd_pr__pfet_01v8 L=4 W=16 nf=1 ad='int((nf+1)/2) * W/nf * 0.29' as='int((nf+2)/2) * W/nf * 0.29'
+ pd='2*int((nf+1)/2) * (W/nf + 0.29)' ps='2*int((nf+2)/2) * (W/nf + 0.29)' nrd='0.29 / W' nrs='0.29 / W'
+ sa=0 sb=0 sd=0 mult=1 m=1
XMdumb45 VDD VDD net21 VDD sky130_fd_pr__pfet_01v8 L=4 W=16 nf=1 ad='int((nf+1)/2) * W/nf * 0.29' as='int((nf+2)/2) * W/nf * 0.29'
+ pd='2*int((nf+1)/2) * (W/nf + 0.29)' ps='2*int((nf+2)/2) * (W/nf + 0.29)' nrd='0.29 / W' nrs='0.29 / W'
+ sa=0 sb=0 sd=0 mult=1 m=1
XMdumb46 VDD VDD net21 VDD sky130_fd_pr__pfet_01v8 L=4 W=16 nf=1 ad='int((nf+1)/2) * W/nf * 0.29' as='int((nf+2)/2) * W/nf * 0.29'
+ pd='2*int((nf+1)/2) * (W/nf + 0.29)' ps='2*int((nf+2)/2) * (W/nf + 0.29)' nrd='0.29 / W' nrs='0.29 / W'
+ sa=0 sb=0 sd=0 mult=1 m=1
XMdumb47 Vgt VDD VDD VDD sky130_fd_pr__pfet_01v8 L=4 W=16 nf=1 ad='int((nf+1)/2) * W/nf * 0.29' as='int((nf+2)/2) * W/nf * 0.29'
+ pd='2*int((nf+1)/2) * (W/nf + 0.29)' ps='2*int((nf+2)/2) * (W/nf + 0.29)' nrd='0.29 / W' nrs='0.29 / W'
+ sa=0 sb=0 sd=0 mult=1 m=1
XMdumb48 Vgt VDD VDD VDD sky130_fd_pr__pfet_01v8 L=4 W=16 nf=1 ad='int((nf+1)/2) * W/nf * 0.29' as='int((nf+2)/2) * W/nf * 0.29'
+ pd='2*int((nf+1)/2) * (W/nf + 0.29)' ps='2*int((nf+2)/2) * (W/nf + 0.29)' nrd='0.29 / W' nrs='0.29 / W'
+ sa=0 sb=0 sd=0 mult=1 m=1
XMdumb49 GND GND net21 GND sky130_fd_pr__nfet_01v8 L=4 W=16 nf=1 ad='int((nf+1)/2) * W/nf * 0.29' as='int((nf+2)/2) * W/nf * 0.29'
+ pd='2*int((nf+1)/2) * (W/nf + 0.29)' ps='2*int((nf+2)/2) * (W/nf + 0.29)' nrd='0.29 / W' nrs='0.29 / W'
+ sa=0 sb=0 sd=0 mult=1 m=1
XMdumb50 GND GND net21 GND sky130_fd_pr__nfet_01v8 L=4 W=16 nf=1 ad='int((nf+1)/2) * W/nf * 0.29' as='int((nf+2)/2) * W/nf * 0.29'
+ pd='2*int((nf+1)/2) * (W/nf + 0.29)' ps='2*int((nf+2)/2) * (W/nf + 0.29)' nrd='0.29 / W' nrs='0.29 / W'
+ sa=0 sb=0 sd=0 mult=1 m=1
XM51 net21 net10 net18 GND sky130_fd_pr__nfet_01v8 L=4 W=16 nf=1 ad='int((nf+1)/2) * W/nf * 0.29' as='int((nf+2)/2) * W/nf * 0.29'
+ pd='2*int((nf+1)/2) * (W/nf + 0.29)' ps='2*int((nf+2)/2) * (W/nf + 0.29)' nrd='0.29 / W' nrs='0.29 / W'
+ sa=0 sb=0 sd=0 mult=1 m=1
XM52 net21 net10 net18 GND sky130_fd_pr__nfet_01v8 L=4 W=16 nf=1 ad='int((nf+1)/2) * W/nf * 0.29' as='int((nf+2)/2) * W/nf * 0.29'
+ pd='2*int((nf+1)/2) * (W/nf + 0.29)' ps='2*int((nf+2)/2) * (W/nf + 0.29)' nrd='0.29 / W' nrs='0.29 / W'
+ sa=0 sb=0 sd=0 mult=1 m=1
XM53 net18 net10 GND GND sky130_fd_pr__nfet_01v8 L=4 W=16 nf=1 ad='int((nf+1)/2) * W/nf * 0.29' as='int((nf+2)/2) * W/nf * 0.29'
+ pd='2*int((nf+1)/2) * (W/nf + 0.29)' ps='2*int((nf+2)/2) * (W/nf + 0.29)' nrd='0.29 / W' nrs='0.29 / W'
+ sa=0 sb=0 sd=0 mult=1 m=1
XM54 net18 net10 GND GND sky130_fd_pr__nfet_01v8 L=4 W=16 nf=1 ad='int((nf+1)/2) * W/nf * 0.29' as='int((nf+2)/2) * W/nf * 0.29'
+ pd='2*int((nf+1)/2) * (W/nf + 0.29)' ps='2*int((nf+2)/2) * (W/nf + 0.29)' nrd='0.29 / W' nrs='0.29 / W'
+ sa=0 sb=0 sd=0 mult=1 m=1
XM55 GND net11 net20 GND sky130_fd_pr__nfet_01v8 L=4 W=16 nf=1 ad='int((nf+1)/2) * W/nf * 0.29' as='int((nf+2)/2) * W/nf * 0.29'
+ pd='2*int((nf+1)/2) * (W/nf + 0.29)' ps='2*int((nf+2)/2) * (W/nf + 0.29)' nrd='0.29 / W' nrs='0.29 / W'
+ sa=0 sb=0 sd=0 mult=1 m=1
XM56 net20 net11 GND GND sky130_fd_pr__nfet_01v8 L=4 W=16 nf=1 ad='int((nf+1)/2) * W/nf * 0.29' as='int((nf+2)/2) * W/nf * 0.29'
+ pd='2*int((nf+1)/2) * (W/nf + 0.29)' ps='2*int((nf+2)/2) * (W/nf + 0.29)' nrd='0.29 / W' nrs='0.29 / W'
+ sa=0 sb=0 sd=0 mult=1 m=1
XM57 net20 net11 Vgt GND sky130_fd_pr__nfet_01v8 L=4 W=16 nf=1 ad='int((nf+1)/2) * W/nf * 0.29' as='int((nf+2)/2) * W/nf * 0.29'
+ pd='2*int((nf+1)/2) * (W/nf + 0.29)' ps='2*int((nf+2)/2) * (W/nf + 0.29)' nrd='0.29 / W' nrs='0.29 / W'
+ sa=0 sb=0 sd=0 mult=1 m=1
XM58 Vgt net11 net20 GND sky130_fd_pr__nfet_01v8 L=4 W=16 nf=1 ad='int((nf+1)/2) * W/nf * 0.29' as='int((nf+2)/2) * W/nf * 0.29'
+ pd='2*int((nf+1)/2) * (W/nf + 0.29)' ps='2*int((nf+2)/2) * (W/nf + 0.29)' nrd='0.29 / W' nrs='0.29 / W'
+ sa=0 sb=0 sd=0 mult=1 m=1
XMdumb59 Vgt GND GND GND sky130_fd_pr__nfet_01v8 L=4 W=16 nf=1 ad='int((nf+1)/2) * W/nf * 0.29' as='int((nf+2)/2) * W/nf * 0.29'
+ pd='2*int((nf+1)/2) * (W/nf + 0.29)' ps='2*int((nf+2)/2) * (W/nf + 0.29)' nrd='0.29 / W' nrs='0.29 / W'
+ sa=0 sb=0 sd=0 mult=1 m=1
XMdumb60 Vgt GND GND GND sky130_fd_pr__nfet_01v8 L=4 W=16 nf=1 ad='int((nf+1)/2) * W/nf * 0.29' as='int((nf+2)/2) * W/nf * 0.29'
+ pd='2*int((nf+1)/2) * (W/nf + 0.29)' ps='2*int((nf+2)/2) * (W/nf + 0.29)' nrd='0.29 / W' nrs='0.29 / W'
+ sa=0 sb=0 sd=0 mult=1 m=1
C1 Vbp GND 10p m=1
**** begin user architecture code

.option wnflag=1
.param MC_SWITCH=0.0
.lib ~/skywater/skywater-pdk/libraries/sky130_fd_pr_ngspice/latest/models/sky130.lib.spice tt


*.control
*dc Vdd 0 1.8 0.01
*save Vibias
*save all
*plot i(Vibias)
*.endc
*.OPTIONS ITL1=1000  ITL2=500 ITL6=500 GMINSTepS=200

.tran 1m 100
.save all


**** end user architecture code
**.ends
.GLOBAL GND
.GLOBAL VDD
.end
